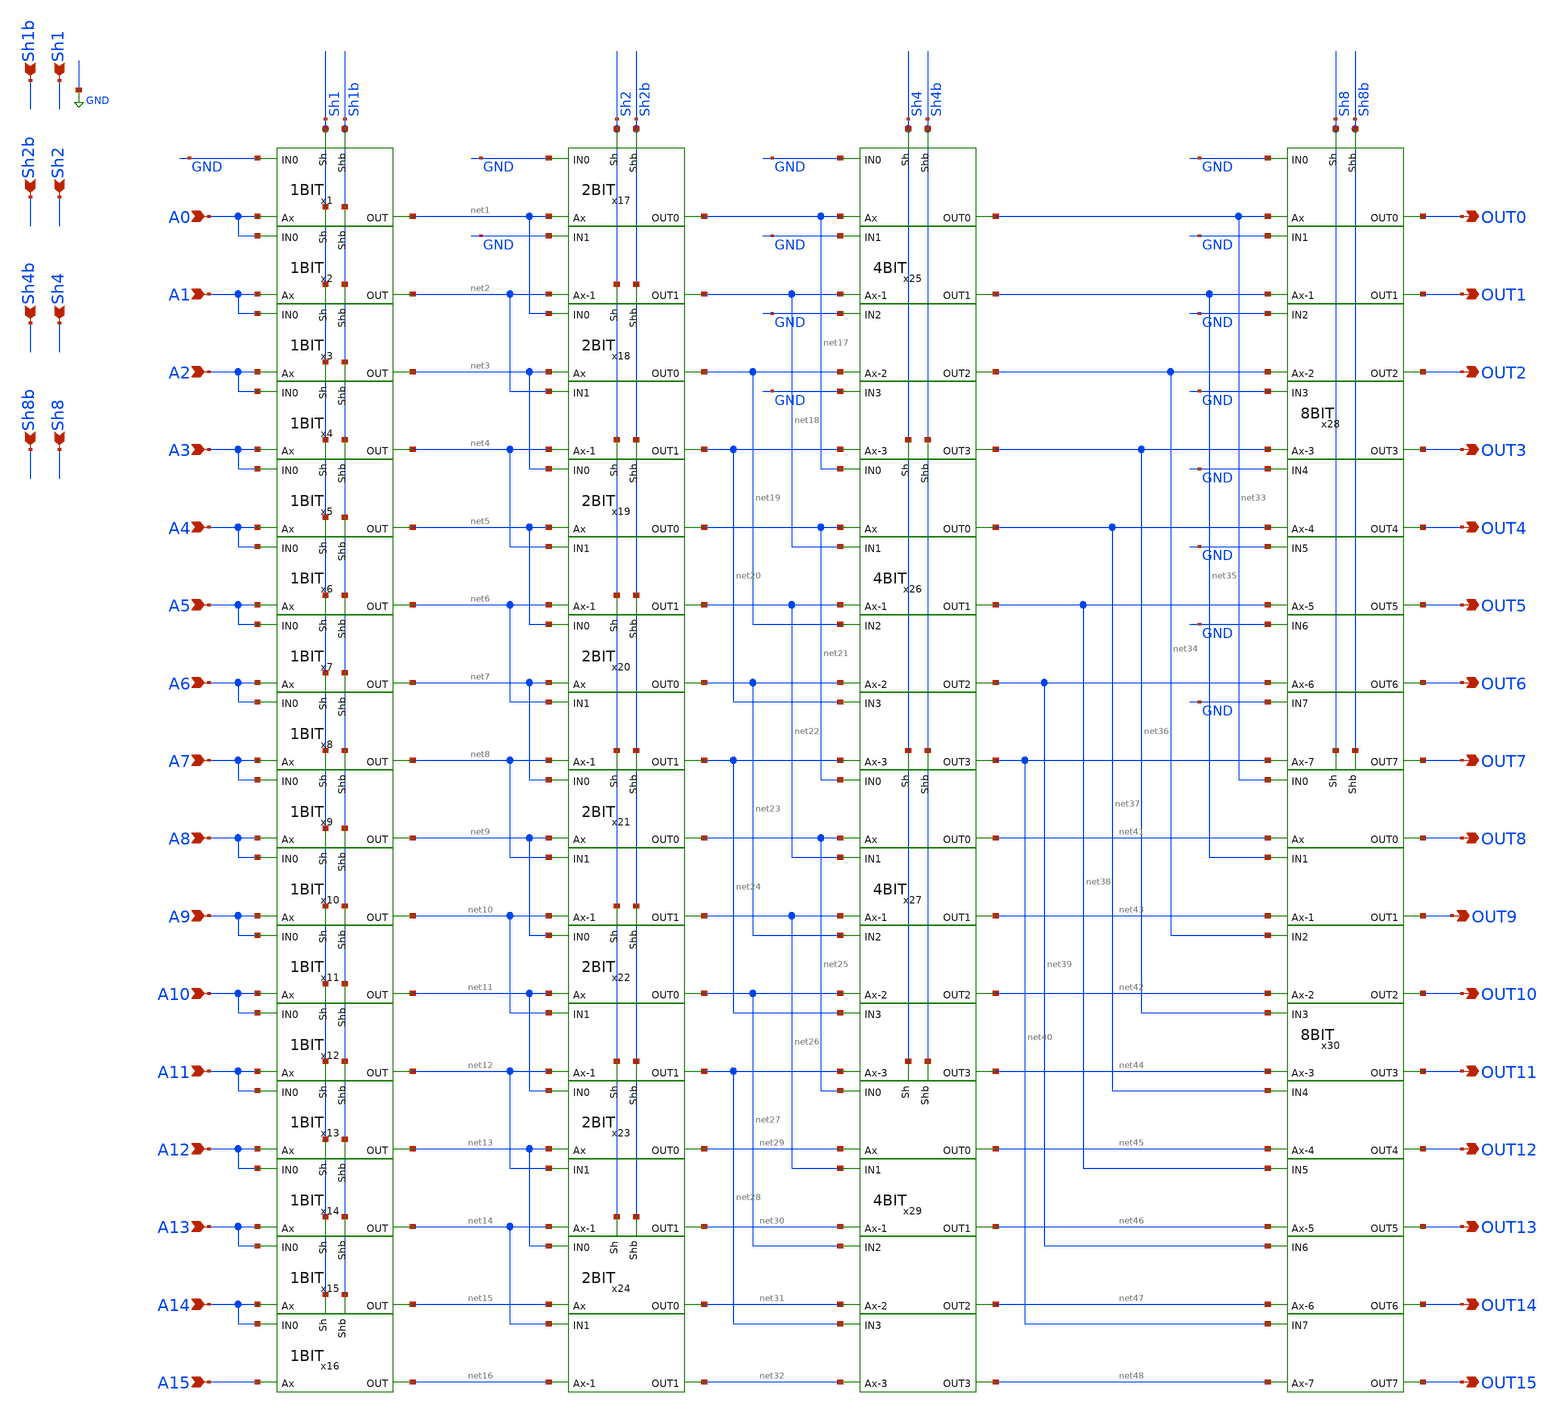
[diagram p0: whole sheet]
** sch_path: SHIFT.sch
**.subckt SHIFT Sh1 Sh1b A0 A1 A2 A3 A4 A5 A6 A7 A8 A9 A10 A11 A12 A13 A14 A15 OUT0 OUT1 OUT2 OUT3
*+ OUT4 OUT5 OUT6 OUT7 OUT8 OUT9 OUT10 OUT11 OUT12 OUT13 OUT14 OUT15 Sh2 Sh2b Sh4 Sh4b Sh8 Sh8b
*.ipin Sh1
*.ipin Sh1b
*.ipin A0
*.ipin A1
*.ipin A2
*.ipin A3
*.ipin A4
*.ipin A5
*.ipin A6
*.ipin A7
*.ipin A8
*.ipin A9
*.ipin A10
*.ipin A11
*.ipin A12
*.ipin A13
*.ipin A14
*.ipin A15
*.opin OUT0
*.opin OUT1
*.opin OUT2
*.opin OUT3
*.opin OUT4
*.opin OUT5
*.opin OUT6
*.opin OUT7
*.opin OUT8
*.opin OUT9
*.opin OUT10
*.opin OUT11
*.opin OUT12
*.opin OUT13
*.opin OUT14
*.opin OUT15
*.ipin Sh2
*.ipin Sh2b
*.ipin Sh4
*.ipin Sh4b
*.ipin Sh8
*.ipin Sh8b
x1 Sh1b Sh1 A0 GND net1 1BIT
x2 Sh1b Sh1 A1 A0 net2 1BIT
x3 Sh1b Sh1 A2 A1 net3 1BIT
x4 Sh1b Sh1 A3 A2 net4 1BIT
x5 Sh1b Sh1 A4 A3 net5 1BIT
x6 Sh1b Sh1 A5 A4 net6 1BIT
x7 Sh1b Sh1 A6 A5 net7 1BIT
x8 Sh1b Sh1 A7 A6 net8 1BIT
x9 Sh1b Sh1 A8 A7 net9 1BIT
x10 Sh1b Sh1 A9 A8 net10 1BIT
x11 Sh1b Sh1 A10 A9 net11 1BIT
x12 Sh1b Sh1 A11 A10 net12 1BIT
x13 Sh1b Sh1 A12 A11 net13 1BIT
x14 Sh1b Sh1 A13 A12 net14 1BIT
x15 Sh1b Sh1 A14 A13 net15 1BIT
x16 Sh1b Sh1 A15 A14 net16 1BIT
x17 Sh2b Sh2 net1 GND net17 net18 GND net2 2BIT
x18 Sh2b Sh2 net3 net1 net19 net20 net2 net4 2BIT
x19 Sh2b Sh2 net5 net3 net21 net22 net4 net6 2BIT
x20 Sh2b Sh2 net7 net5 net23 net24 net6 net8 2BIT
x21 Sh2b Sh2 net9 net7 net25 net26 net8 net10 2BIT
x22 Sh2b Sh2 net11 net9 net27 net28 net10 net12 2BIT
x23 Sh2b Sh2 net13 net11 net29 net30 net12 net14 2BIT
x24 Sh2b Sh2 net15 net13 net31 net32 net14 net16 2BIT
x25 Sh4b Sh4 GND net17 net33 net35 net34 net36 GND net18 GND net19 GND net20 4BIT
x26 Sh4b Sh4 net17 net21 net37 net38 net39 net40 net18 net22 net19 net23 net20 net24 4BIT
x27 Sh4b Sh4 net21 net25 net41 net43 net42 net44 net22 net26 net23 net27 net24 net28 4BIT
x29 Sh4b Sh4 net25 net29 net45 net46 net47 net48 net26 net30 net27 net31 net28 net32 4BIT
x28 Sh8b Sh8 net33 GND OUT0 OUT1 OUT2 OUT3 net35 GND GND net34 GND net36 net37 GND OUT4 OUT5 OUT6
+ OUT7 GND net38 GND net39 GND net40 8BIT
x30 Sh8b Sh8 net41 net33 OUT8 OUT9 OUT10 OUT11 net43 net35 net34 net42 net36 net44 net45 net37 OUT12
+ OUT13 OUT14 OUT15 net38 net46 net39 net47 net40 net48 8BIT
**.ends
.GLOBAL GND
.end
